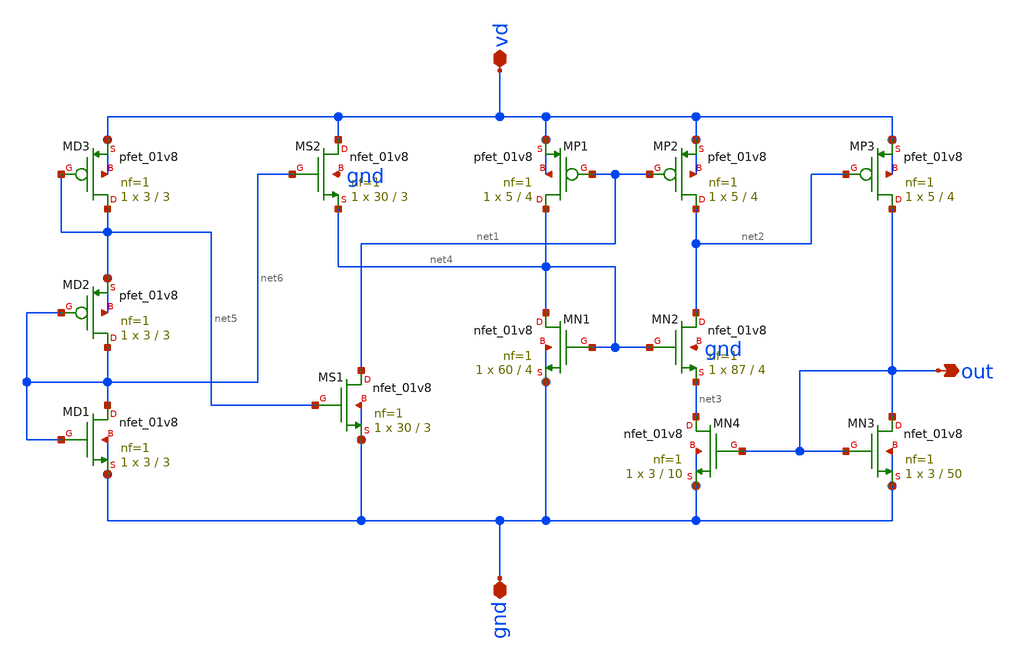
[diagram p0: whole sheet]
** sch_path: bandgap-ref/xschem/bandgap-ref.sch
**.subckt bandgap-ref vd gnd out
*.iopin vd
*.iopin gnd
*.opin out
XMN1 net4 net4 gnd gnd sky130_fd_pr__nfet_01v8 L=4 W=60 nf=1 ad='int((nf+1)/2) * W/nf * 0.29' as='int((nf+2)/2) * W/nf * 0.29'
+ pd='2*int((nf+1)/2) * (W/nf + 0.29)' ps='2*int((nf+2)/2) * (W/nf + 0.29)' nrd='0.29 / W' nrs='0.29 / W'
+ sa=0 sb=0 sd=0 mult=1 m=1
XMP1 net4 net1 vd vd sky130_fd_pr__pfet_01v8 L=4 W=5 nf=1 ad='int((nf+1)/2) * W/nf * 0.29' as='int((nf+2)/2) * W/nf * 0.29'
+ pd='2*int((nf+1)/2) * (W/nf + 0.29)' ps='2*int((nf+2)/2) * (W/nf + 0.29)' nrd='0.29 / W' nrs='0.29 / W'
+ sa=0 sb=0 sd=0 mult=1 m=1
XMP2 net2 net1 vd vd sky130_fd_pr__pfet_01v8 L=4 W=5 nf=1 ad='int((nf+1)/2) * W/nf * 0.29' as='int((nf+2)/2) * W/nf * 0.29'
+ pd='2*int((nf+1)/2) * (W/nf + 0.29)' ps='2*int((nf+2)/2) * (W/nf + 0.29)' nrd='0.29 / W' nrs='0.29 / W'
+ sa=0 sb=0 sd=0 mult=1 m=1
XMP3 out net2 vd vd sky130_fd_pr__pfet_01v8 L=4 W=5 nf=1 ad='int((nf+1)/2) * W/nf * 0.29' as='int((nf+2)/2) * W/nf * 0.29'
+ pd='2*int((nf+1)/2) * (W/nf + 0.29)' ps='2*int((nf+2)/2) * (W/nf + 0.29)' nrd='0.29 / W' nrs='0.29 / W'
+ sa=0 sb=0 sd=0 mult=1 m=1
XMN2 net2 net4 net3 gnd sky130_fd_pr__nfet_01v8 L=4 W=87 nf=1 ad='int((nf+1)/2) * W/nf * 0.29' as='int((nf+2)/2) * W/nf * 0.29'
+ pd='2*int((nf+1)/2) * (W/nf + 0.29)' ps='2*int((nf+2)/2) * (W/nf + 0.29)' nrd='0.29 / W' nrs='0.29 / W'
+ sa=0 sb=0 sd=0 mult=1 m=1
XMN3 out out gnd gnd sky130_fd_pr__nfet_01v8 L=50 W=3 nf=1 ad='int((nf+1)/2) * W/nf * 0.29' as='int((nf+2)/2) * W/nf * 0.29'
+ pd='2*int((nf+1)/2) * (W/nf + 0.29)' ps='2*int((nf+2)/2) * (W/nf + 0.29)' nrd='0.29 / W' nrs='0.29 / W'
+ sa=0 sb=0 sd=0 mult=1 m=1
XMN4 net3 out gnd gnd sky130_fd_pr__nfet_01v8 L=10 W=3 nf=1 ad='int((nf+1)/2) * W/nf * 0.29' as='int((nf+2)/2) * W/nf * 0.29'
+ pd='2*int((nf+1)/2) * (W/nf + 0.29)' ps='2*int((nf+2)/2) * (W/nf + 0.29)' nrd='0.29 / W' nrs='0.29 / W'
+ sa=0 sb=0 sd=0 mult=1 m=1
XMS1 net1 net5 gnd gnd sky130_fd_pr__nfet_01v8 L=3 W=30 nf=1 ad='int((nf+1)/2) * W/nf * 0.29' as='int((nf+2)/2) * W/nf * 0.29'
+ pd='2*int((nf+1)/2) * (W/nf + 0.29)' ps='2*int((nf+2)/2) * (W/nf + 0.29)' nrd='0.29 / W' nrs='0.29 / W'
+ sa=0 sb=0 sd=0 mult=1 m=1
XMD3 net5 net5 vd vd sky130_fd_pr__pfet_01v8 L=3 W=3 nf=1 ad='int((nf+1)/2) * W/nf * 0.29' as='int((nf+2)/2) * W/nf * 0.29'
+ pd='2*int((nf+1)/2) * (W/nf + 0.29)' ps='2*int((nf+2)/2) * (W/nf + 0.29)' nrd='0.29 / W' nrs='0.29 / W'
+ sa=0 sb=0 sd=0 mult=1 m=1
XMD2 net6 net6 net5 net5 sky130_fd_pr__pfet_01v8 L=3 W=3 nf=1 ad='int((nf+1)/2) * W/nf * 0.29' as='int((nf+2)/2) * W/nf * 0.29'
+ pd='2*int((nf+1)/2) * (W/nf + 0.29)' ps='2*int((nf+2)/2) * (W/nf + 0.29)' nrd='0.29 / W' nrs='0.29 / W'
+ sa=0 sb=0 sd=0 mult=1 m=1
XMD1 net6 net6 gnd gnd sky130_fd_pr__nfet_01v8 L=3 W=3 nf=1 ad='int((nf+1)/2) * W/nf * 0.29' as='int((nf+2)/2) * W/nf * 0.29'
+ pd='2*int((nf+1)/2) * (W/nf + 0.29)' ps='2*int((nf+2)/2) * (W/nf + 0.29)' nrd='0.29 / W' nrs='0.29 / W'
+ sa=0 sb=0 sd=0 mult=1 m=1
XMS2 vd net6 net4 gnd sky130_fd_pr__nfet_01v8 L=3 W=30 nf=1 ad='int((nf+1)/2) * W/nf * 0.29' as='int((nf+2)/2) * W/nf * 0.29'
+ pd='2*int((nf+1)/2) * (W/nf + 0.29)' ps='2*int((nf+2)/2) * (W/nf + 0.29)' nrd='0.29 / W' nrs='0.29 / W'
+ sa=0 sb=0 sd=0 mult=1 m=1
**.ends
.end
